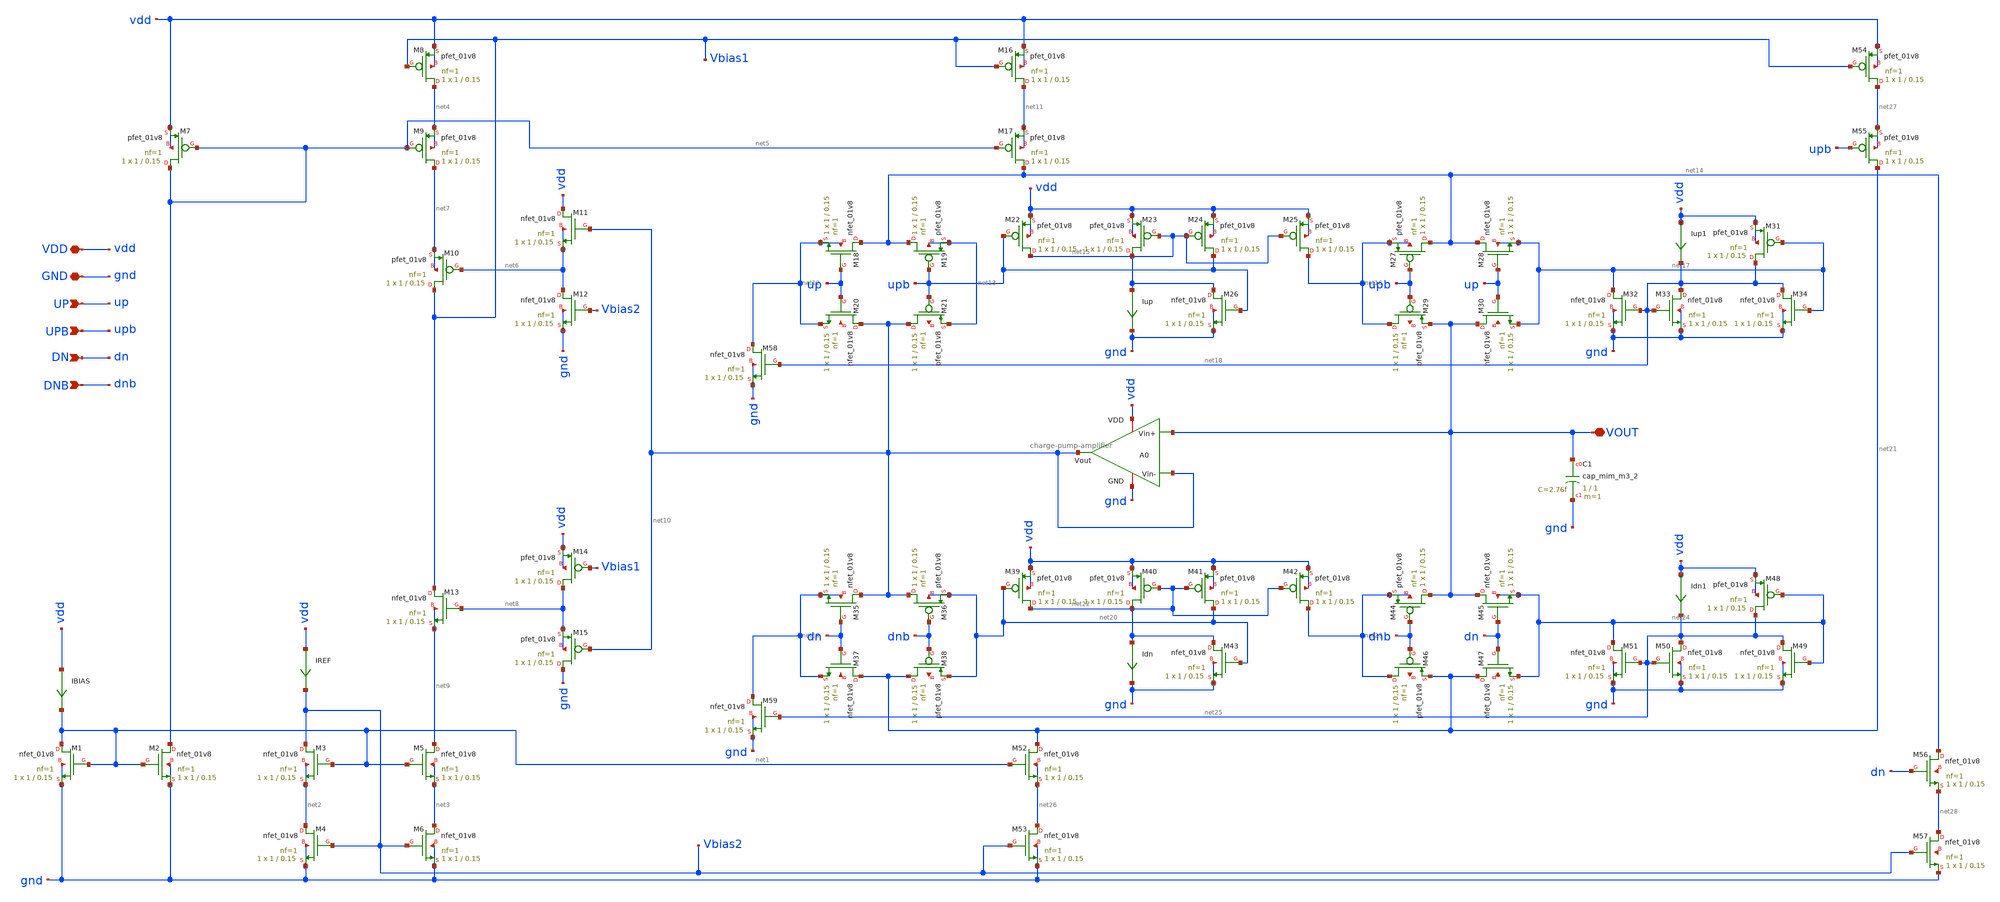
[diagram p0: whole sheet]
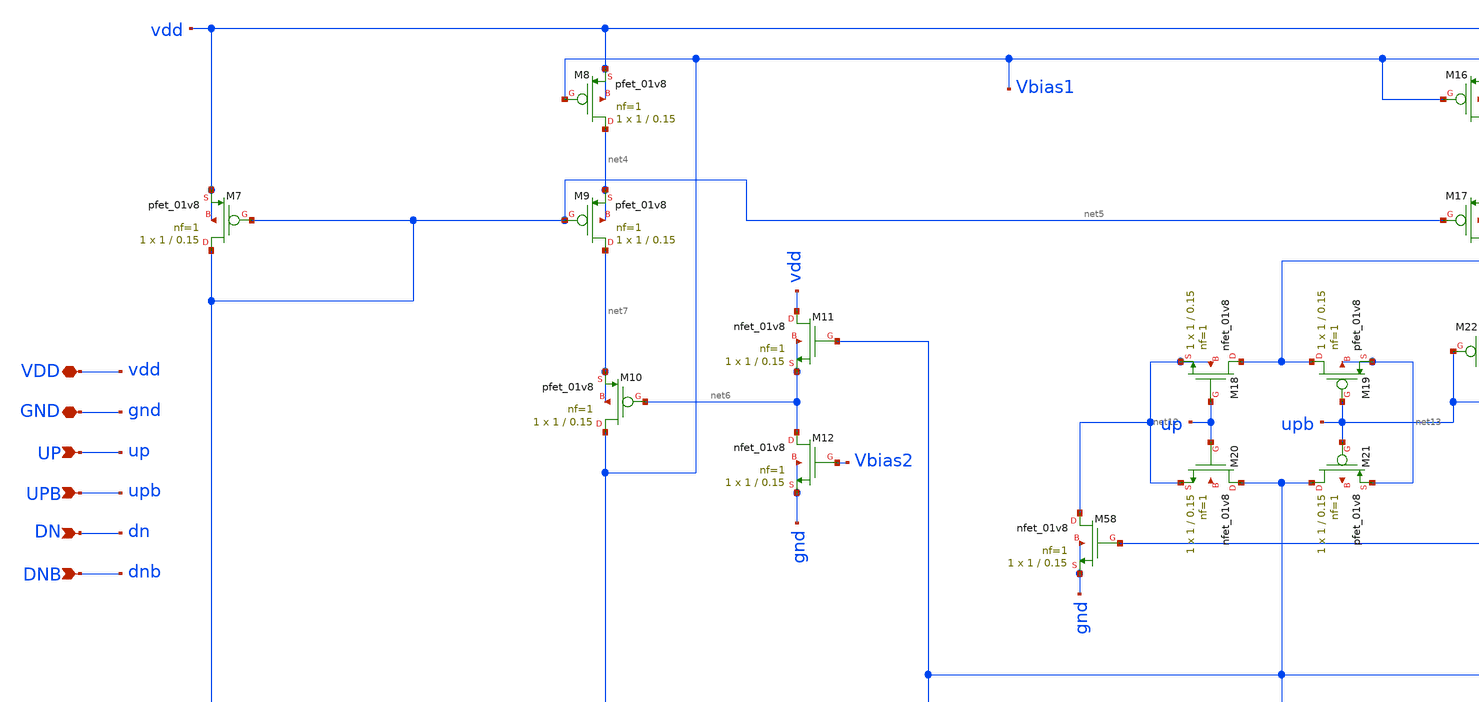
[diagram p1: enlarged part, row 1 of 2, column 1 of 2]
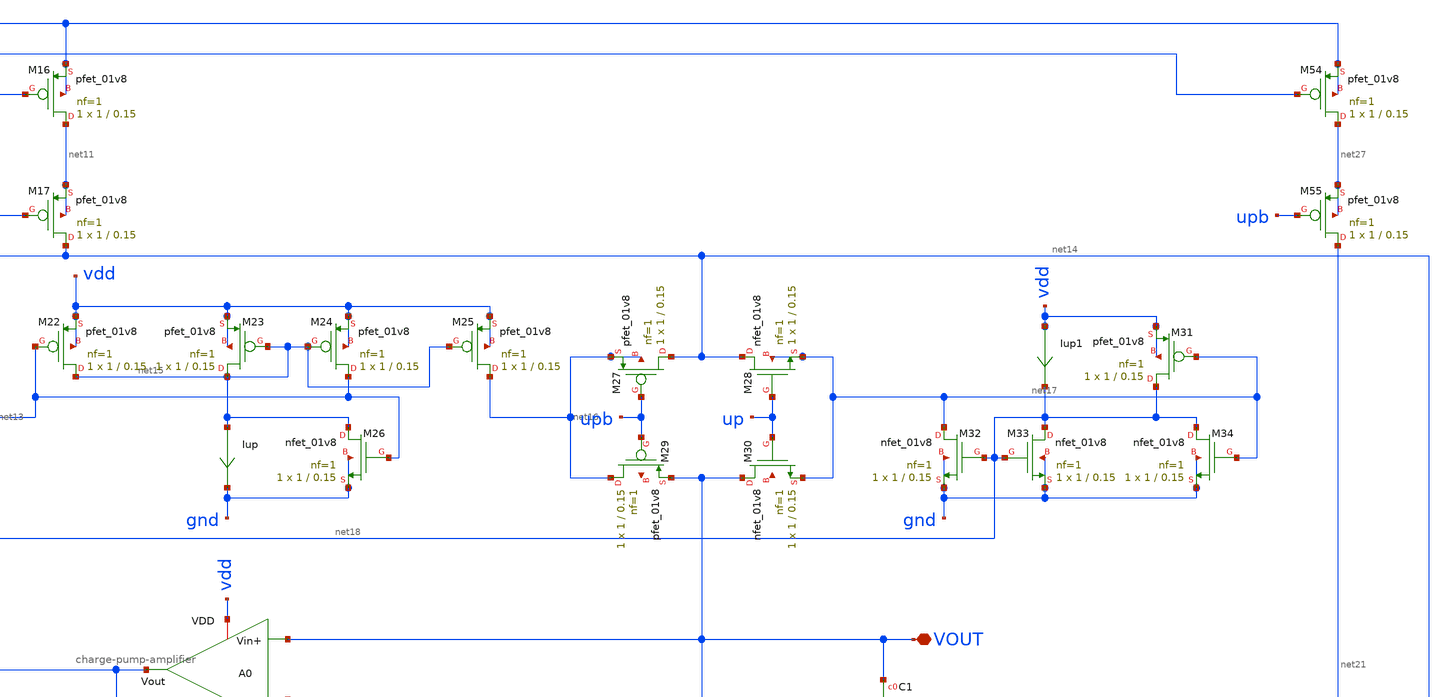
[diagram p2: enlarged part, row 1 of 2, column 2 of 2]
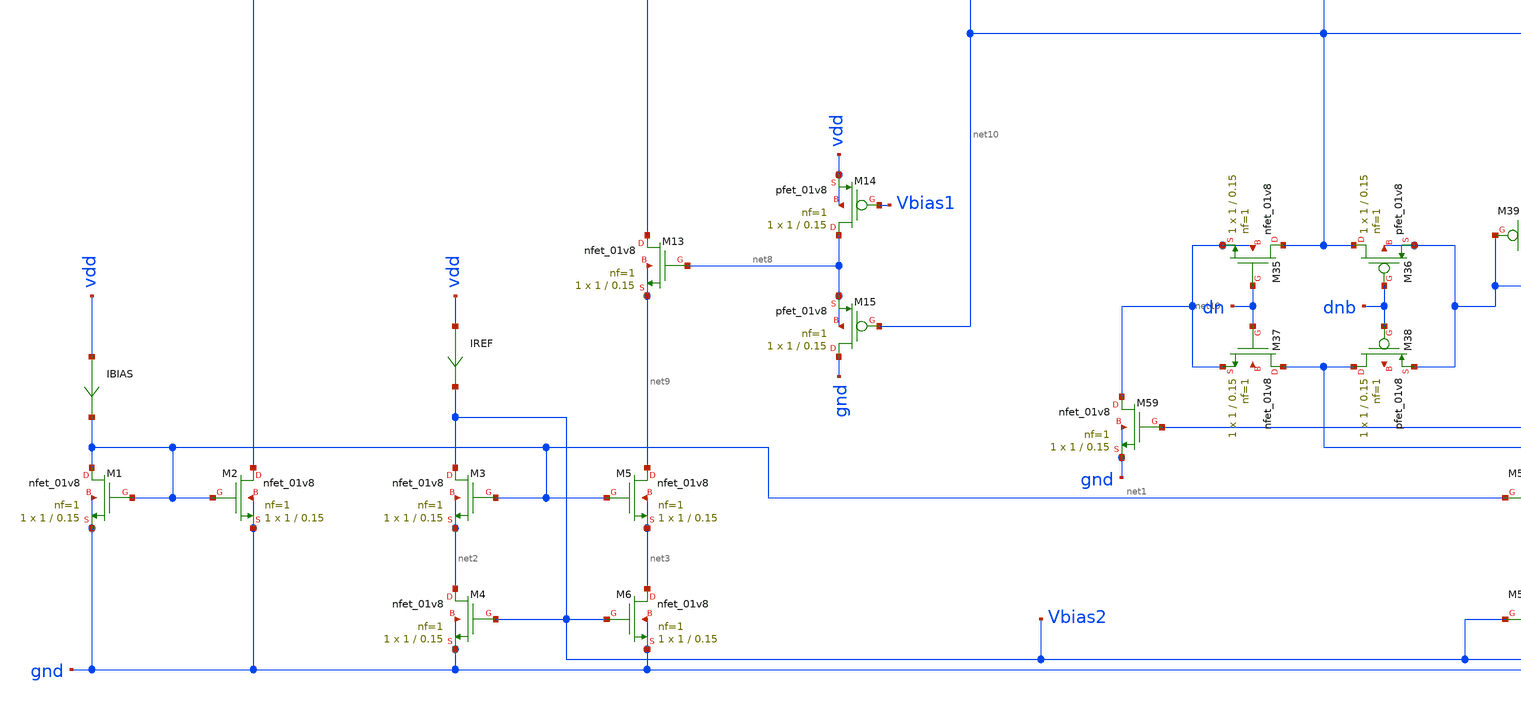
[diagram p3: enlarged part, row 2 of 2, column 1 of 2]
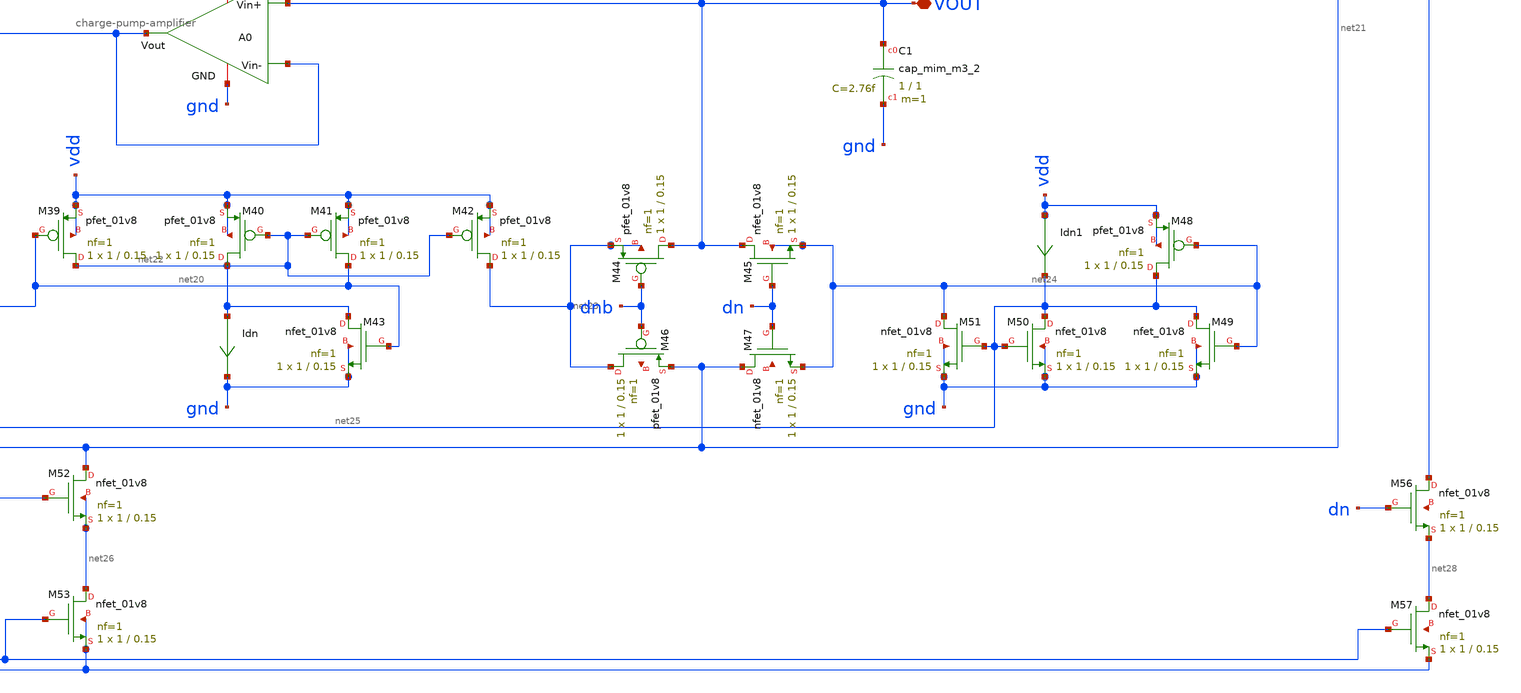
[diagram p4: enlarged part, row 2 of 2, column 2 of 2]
** sch_path: charge-pump/charge-pump.sch
**.subckt charge-pump VOUT DN VDD GND DNB UPB UP
*.iopin VOUT
*.ipin DN
*.iopin VDD
*.iopin GND
*.ipin DNB
*.ipin UPB
*.ipin UP
XM1 net1 net1 gnd gnd sky130_fd_pr__nfet_01v8 L=0.15 W=1 nf=1 ad='int((nf+1)/2) * W/nf * 0.29' as='int((nf+2)/2) * W/nf * 0.29'
+ pd='2*int((nf+1)/2) * (W/nf + 0.29)' ps='2*int((nf+2)/2) * (W/nf + 0.29)' nrd='0.29 / W' nrs='0.29 / W'
+ sa=0 sb=0 sd=0 mult=1 m=1
XM2 net5 net1 gnd gnd sky130_fd_pr__nfet_01v8 L=0.15 W=1 nf=1 ad='int((nf+1)/2) * W/nf * 0.29' as='int((nf+2)/2) * W/nf * 0.29'
+ pd='2*int((nf+1)/2) * (W/nf + 0.29)' ps='2*int((nf+2)/2) * (W/nf + 0.29)' nrd='0.29 / W' nrs='0.29 / W'
+ sa=0 sb=0 sd=0 mult=1 m=1
XM3 Vbias2 net1 net2 net2 sky130_fd_pr__nfet_01v8 L=0.15 W=1 nf=1 ad='int((nf+1)/2) * W/nf * 0.29' as='int((nf+2)/2) * W/nf * 0.29'
+ pd='2*int((nf+1)/2) * (W/nf + 0.29)' ps='2*int((nf+2)/2) * (W/nf + 0.29)' nrd='0.29 / W' nrs='0.29 / W'
+ sa=0 sb=0 sd=0 mult=1 m=1
XM4 net2 Vbias2 gnd gnd sky130_fd_pr__nfet_01v8 L=0.15 W=1 nf=1 ad='int((nf+1)/2) * W/nf * 0.29' as='int((nf+2)/2) * W/nf * 0.29'
+ pd='2*int((nf+1)/2) * (W/nf + 0.29)' ps='2*int((nf+2)/2) * (W/nf + 0.29)' nrd='0.29 / W' nrs='0.29 / W'
+ sa=0 sb=0 sd=0 mult=1 m=1
XM5 net9 net1 net3 net3 sky130_fd_pr__nfet_01v8 L=0.15 W=1 nf=1 ad='int((nf+1)/2) * W/nf * 0.29' as='int((nf+2)/2) * W/nf * 0.29'
+ pd='2*int((nf+1)/2) * (W/nf + 0.29)' ps='2*int((nf+2)/2) * (W/nf + 0.29)' nrd='0.29 / W' nrs='0.29 / W'
+ sa=0 sb=0 sd=0 mult=1 m=1
XM6 net3 Vbias2 gnd gnd sky130_fd_pr__nfet_01v8 L=0.15 W=1 nf=1 ad='int((nf+1)/2) * W/nf * 0.29' as='int((nf+2)/2) * W/nf * 0.29'
+ pd='2*int((nf+1)/2) * (W/nf + 0.29)' ps='2*int((nf+2)/2) * (W/nf + 0.29)' nrd='0.29 / W' nrs='0.29 / W'
+ sa=0 sb=0 sd=0 mult=1 m=1
XM7 net5 net5 vdd vdd sky130_fd_pr__pfet_01v8 L=0.15 W=1 nf=1 ad='int((nf+1)/2) * W/nf * 0.29' as='int((nf+2)/2) * W/nf * 0.29'
+ pd='2*int((nf+1)/2) * (W/nf + 0.29)' ps='2*int((nf+2)/2) * (W/nf + 0.29)' nrd='0.29 / W' nrs='0.29 / W'
+ sa=0 sb=0 sd=0 mult=1 m=1
XM8 net4 Vbias1 vdd vdd sky130_fd_pr__pfet_01v8 L=0.15 W=1 nf=1 ad='int((nf+1)/2) * W/nf * 0.29' as='int((nf+2)/2) * W/nf * 0.29'
+ pd='2*int((nf+1)/2) * (W/nf + 0.29)' ps='2*int((nf+2)/2) * (W/nf + 0.29)' nrd='0.29 / W' nrs='0.29 / W'
+ sa=0 sb=0 sd=0 mult=1 m=1
XM9 net7 net5 net4 net4 sky130_fd_pr__pfet_01v8 L=0.15 W=1 nf=1 ad='int((nf+1)/2) * W/nf * 0.29' as='int((nf+2)/2) * W/nf * 0.29'
+ pd='2*int((nf+1)/2) * (W/nf + 0.29)' ps='2*int((nf+2)/2) * (W/nf + 0.29)' nrd='0.29 / W' nrs='0.29 / W'
+ sa=0 sb=0 sd=0 mult=1 m=1
XM10 Vbias1 net6 net7 net7 sky130_fd_pr__pfet_01v8 L=0.15 W=1 nf=1 ad='int((nf+1)/2) * W/nf * 0.29' as='int((nf+2)/2) * W/nf * 0.29'
+ pd='2*int((nf+1)/2) * (W/nf + 0.29)' ps='2*int((nf+2)/2) * (W/nf + 0.29)' nrd='0.29 / W' nrs='0.29 / W'
+ sa=0 sb=0 sd=0 mult=1 m=1
XM11 vdd net10 net6 net6 sky130_fd_pr__nfet_01v8 L=0.15 W=1 nf=1 ad='int((nf+1)/2) * W/nf * 0.29' as='int((nf+2)/2) * W/nf * 0.29'
+ pd='2*int((nf+1)/2) * (W/nf + 0.29)' ps='2*int((nf+2)/2) * (W/nf + 0.29)' nrd='0.29 / W' nrs='0.29 / W'
+ sa=0 sb=0 sd=0 mult=1 m=1
XM12 net6 Vbias2 gnd gnd sky130_fd_pr__nfet_01v8 L=0.15 W=1 nf=1 ad='int((nf+1)/2) * W/nf * 0.29' as='int((nf+2)/2) * W/nf * 0.29'
+ pd='2*int((nf+1)/2) * (W/nf + 0.29)' ps='2*int((nf+2)/2) * (W/nf + 0.29)' nrd='0.29 / W' nrs='0.29 / W'
+ sa=0 sb=0 sd=0 mult=1 m=1
XM13 Vbias1 net8 net9 net9 sky130_fd_pr__nfet_01v8 L=0.15 W=1 nf=1 ad='int((nf+1)/2) * W/nf * 0.29' as='int((nf+2)/2) * W/nf * 0.29'
+ pd='2*int((nf+1)/2) * (W/nf + 0.29)' ps='2*int((nf+2)/2) * (W/nf + 0.29)' nrd='0.29 / W' nrs='0.29 / W'
+ sa=0 sb=0 sd=0 mult=1 m=1
XM14 net8 Vbias1 vdd vdd sky130_fd_pr__pfet_01v8 L=0.15 W=1 nf=1 ad='int((nf+1)/2) * W/nf * 0.29' as='int((nf+2)/2) * W/nf * 0.29'
+ pd='2*int((nf+1)/2) * (W/nf + 0.29)' ps='2*int((nf+2)/2) * (W/nf + 0.29)' nrd='0.29 / W' nrs='0.29 / W'
+ sa=0 sb=0 sd=0 mult=1 m=1
XM15 gnd net10 net8 net8 sky130_fd_pr__pfet_01v8 L=0.15 W=1 nf=1 ad='int((nf+1)/2) * W/nf * 0.29' as='int((nf+2)/2) * W/nf * 0.29'
+ pd='2*int((nf+1)/2) * (W/nf + 0.29)' ps='2*int((nf+2)/2) * (W/nf + 0.29)' nrd='0.29 / W' nrs='0.29 / W'
+ sa=0 sb=0 sd=0 mult=1 m=1
XM16 net11 Vbias1 vdd vdd sky130_fd_pr__pfet_01v8 L=0.15 W=1 nf=1 ad='int((nf+1)/2) * W/nf * 0.29' as='int((nf+2)/2) * W/nf * 0.29'
+ pd='2*int((nf+1)/2) * (W/nf + 0.29)' ps='2*int((nf+2)/2) * (W/nf + 0.29)' nrd='0.29 / W' nrs='0.29 / W'
+ sa=0 sb=0 sd=0 mult=1 m=1
XM17 net14 net5 net11 net11 sky130_fd_pr__pfet_01v8 L=0.15 W=1 nf=1 ad='int((nf+1)/2) * W/nf * 0.29'
+ as='int((nf+2)/2) * W/nf * 0.29' pd='2*int((nf+1)/2) * (W/nf + 0.29)' ps='2*int((nf+2)/2) * (W/nf + 0.29)'
+ nrd='0.29 / W' nrs='0.29 / W' sa=0 sb=0 sd=0 mult=1 m=1
XM18 net14 up net12 net12 sky130_fd_pr__nfet_01v8 L=0.15 W=1 nf=1 ad='int((nf+1)/2) * W/nf * 0.29' as='int((nf+2)/2) * W/nf * 0.29'
+ pd='2*int((nf+1)/2) * (W/nf + 0.29)' ps='2*int((nf+2)/2) * (W/nf + 0.29)' nrd='0.29 / W' nrs='0.29 / W'
+ sa=0 sb=0 sd=0 mult=1 m=1
XM19 net14 upb net13 net13 sky130_fd_pr__pfet_01v8 L=0.15 W=1 nf=1 ad='int((nf+1)/2) * W/nf * 0.29' as='int((nf+2)/2) * W/nf * 0.29'
+ pd='2*int((nf+1)/2) * (W/nf + 0.29)' ps='2*int((nf+2)/2) * (W/nf + 0.29)' nrd='0.29 / W' nrs='0.29 / W'
+ sa=0 sb=0 sd=0 mult=1 m=1
XM20 net10 up net12 net29 sky130_fd_pr__nfet_01v8 L=0.15 W=1 nf=1 ad='int((nf+1)/2) * W/nf * 0.29' as='int((nf+2)/2) * W/nf * 0.29'
+ pd='2*int((nf+1)/2) * (W/nf + 0.29)' ps='2*int((nf+2)/2) * (W/nf + 0.29)' nrd='0.29 / W' nrs='0.29 / W'
+ sa=0 sb=0 sd=0 mult=1 m=1
XM21 net10 upb net13 net30 sky130_fd_pr__pfet_01v8 L=0.15 W=1 nf=1 ad='int((nf+1)/2) * W/nf * 0.29' as='int((nf+2)/2) * W/nf * 0.29'
+ pd='2*int((nf+1)/2) * (W/nf + 0.29)' ps='2*int((nf+2)/2) * (W/nf + 0.29)' nrd='0.29 / W' nrs='0.29 / W'
+ sa=0 sb=0 sd=0 mult=1 m=1
XM22 net15 upb vdd vdd sky130_fd_pr__pfet_01v8 L=0.15 W=1 nf=1 ad='int((nf+1)/2) * W/nf * 0.29' as='int((nf+2)/2) * W/nf * 0.29'
+ pd='2*int((nf+1)/2) * (W/nf + 0.29)' ps='2*int((nf+2)/2) * (W/nf + 0.29)' nrd='0.29 / W' nrs='0.29 / W'
+ sa=0 sb=0 sd=0 mult=1 m=1
XM23 net15 net15 vdd vdd sky130_fd_pr__pfet_01v8 L=0.15 W=1 nf=1 ad='int((nf+1)/2) * W/nf * 0.29' as='int((nf+2)/2) * W/nf * 0.29'
+ pd='2*int((nf+1)/2) * (W/nf + 0.29)' ps='2*int((nf+2)/2) * (W/nf + 0.29)' nrd='0.29 / W' nrs='0.29 / W'
+ sa=0 sb=0 sd=0 mult=1 m=1
XM24 upb net15 vdd vdd sky130_fd_pr__pfet_01v8 L=0.15 W=1 nf=1 ad='int((nf+1)/2) * W/nf * 0.29' as='int((nf+2)/2) * W/nf * 0.29'
+ pd='2*int((nf+1)/2) * (W/nf + 0.29)' ps='2*int((nf+2)/2) * (W/nf + 0.29)' nrd='0.29 / W' nrs='0.29 / W'
+ sa=0 sb=0 sd=0 mult=1 m=1
XM25 net16 net15 vdd vdd sky130_fd_pr__pfet_01v8 L=0.15 W=1 nf=1 ad='int((nf+1)/2) * W/nf * 0.29' as='int((nf+2)/2) * W/nf * 0.29'
+ pd='2*int((nf+1)/2) * (W/nf + 0.29)' ps='2*int((nf+2)/2) * (W/nf + 0.29)' nrd='0.29 / W' nrs='0.29 / W'
+ sa=0 sb=0 sd=0 mult=1 m=1
XM26 net15 upb gnd gnd sky130_fd_pr__nfet_01v8 L=0.15 W=1 nf=1 ad='int((nf+1)/2) * W/nf * 0.29' as='int((nf+2)/2) * W/nf * 0.29'
+ pd='2*int((nf+1)/2) * (W/nf + 0.29)' ps='2*int((nf+2)/2) * (W/nf + 0.29)' nrd='0.29 / W' nrs='0.29 / W'
+ sa=0 sb=0 sd=0 mult=1 m=1
XM31 net18 net17 vdd vdd sky130_fd_pr__pfet_01v8 L=0.15 W=1 nf=1 ad='int((nf+1)/2) * W/nf * 0.29' as='int((nf+2)/2) * W/nf * 0.29'
+ pd='2*int((nf+1)/2) * (W/nf + 0.29)' ps='2*int((nf+2)/2) * (W/nf + 0.29)' nrd='0.29 / W' nrs='0.29 / W'
+ sa=0 sb=0 sd=0 mult=1 m=1
XM32 net17 net18 gnd gnd sky130_fd_pr__nfet_01v8 L=0.15 W=1 nf=1 ad='int((nf+1)/2) * W/nf * 0.29' as='int((nf+2)/2) * W/nf * 0.29'
+ pd='2*int((nf+1)/2) * (W/nf + 0.29)' ps='2*int((nf+2)/2) * (W/nf + 0.29)' nrd='0.29 / W' nrs='0.29 / W'
+ sa=0 sb=0 sd=0 mult=1 m=1
XM33 net18 net18 gnd gnd sky130_fd_pr__nfet_01v8 L=0.15 W=1 nf=1 ad='int((nf+1)/2) * W/nf * 0.29' as='int((nf+2)/2) * W/nf * 0.29'
+ pd='2*int((nf+1)/2) * (W/nf + 0.29)' ps='2*int((nf+2)/2) * (W/nf + 0.29)' nrd='0.29 / W' nrs='0.29 / W'
+ sa=0 sb=0 sd=0 mult=1 m=1
XM34 net18 net17 gnd gnd sky130_fd_pr__nfet_01v8 L=0.15 W=1 nf=1 ad='int((nf+1)/2) * W/nf * 0.29' as='int((nf+2)/2) * W/nf * 0.29'
+ pd='2*int((nf+1)/2) * (W/nf + 0.29)' ps='2*int((nf+2)/2) * (W/nf + 0.29)' nrd='0.29 / W' nrs='0.29 / W'
+ sa=0 sb=0 sd=0 mult=1 m=1
XM27 net14 upb net16 net16 sky130_fd_pr__pfet_01v8 L=0.15 W=1 nf=1 ad='int((nf+1)/2) * W/nf * 0.29' as='int((nf+2)/2) * W/nf * 0.29'
+ pd='2*int((nf+1)/2) * (W/nf + 0.29)' ps='2*int((nf+2)/2) * (W/nf + 0.29)' nrd='0.29 / W' nrs='0.29 / W'
+ sa=0 sb=0 sd=0 mult=1 m=1
XM28 net14 up net17 net17 sky130_fd_pr__nfet_01v8 L=0.15 W=1 nf=1 ad='int((nf+1)/2) * W/nf * 0.29' as='int((nf+2)/2) * W/nf * 0.29'
+ pd='2*int((nf+1)/2) * (W/nf + 0.29)' ps='2*int((nf+2)/2) * (W/nf + 0.29)' nrd='0.29 / W' nrs='0.29 / W'
+ sa=0 sb=0 sd=0 mult=1 m=1
XM29 net16 upb VOUT net31 sky130_fd_pr__pfet_01v8 L=0.15 W=1 nf=1 ad='int((nf+1)/2) * W/nf * 0.29' as='int((nf+2)/2) * W/nf * 0.29'
+ pd='2*int((nf+1)/2) * (W/nf + 0.29)' ps='2*int((nf+2)/2) * (W/nf + 0.29)' nrd='0.29 / W' nrs='0.29 / W'
+ sa=0 sb=0 sd=0 mult=1 m=1
XM30 VOUT up net17 net32 sky130_fd_pr__nfet_01v8 L=0.15 W=1 nf=1 ad='int((nf+1)/2) * W/nf * 0.29' as='int((nf+2)/2) * W/nf * 0.29'
+ pd='2*int((nf+1)/2) * (W/nf + 0.29)' ps='2*int((nf+2)/2) * (W/nf + 0.29)' nrd='0.29 / W' nrs='0.29 / W'
+ sa=0 sb=0 sd=0 mult=1 m=1
XM35 net10 dn net19 net19 sky130_fd_pr__nfet_01v8 L=0.15 W=1 nf=1 ad='int((nf+1)/2) * W/nf * 0.29' as='int((nf+2)/2) * W/nf * 0.29'
+ pd='2*int((nf+1)/2) * (W/nf + 0.29)' ps='2*int((nf+2)/2) * (W/nf + 0.29)' nrd='0.29 / W' nrs='0.29 / W'
+ sa=0 sb=0 sd=0 mult=1 m=1
XM36 net10 dnb net20 net20 sky130_fd_pr__pfet_01v8 L=0.15 W=1 nf=1 ad='int((nf+1)/2) * W/nf * 0.29' as='int((nf+2)/2) * W/nf * 0.29'
+ pd='2*int((nf+1)/2) * (W/nf + 0.29)' ps='2*int((nf+2)/2) * (W/nf + 0.29)' nrd='0.29 / W' nrs='0.29 / W'
+ sa=0 sb=0 sd=0 mult=1 m=1
XM37 net21 dn net19 net33 sky130_fd_pr__nfet_01v8 L=0.15 W=1 nf=1 ad='int((nf+1)/2) * W/nf * 0.29' as='int((nf+2)/2) * W/nf * 0.29'
+ pd='2*int((nf+1)/2) * (W/nf + 0.29)' ps='2*int((nf+2)/2) * (W/nf + 0.29)' nrd='0.29 / W' nrs='0.29 / W'
+ sa=0 sb=0 sd=0 mult=1 m=1
XM38 net21 dnb net20 net34 sky130_fd_pr__pfet_01v8 L=0.15 W=1 nf=1 ad='int((nf+1)/2) * W/nf * 0.29' as='int((nf+2)/2) * W/nf * 0.29'
+ pd='2*int((nf+1)/2) * (W/nf + 0.29)' ps='2*int((nf+2)/2) * (W/nf + 0.29)' nrd='0.29 / W' nrs='0.29 / W'
+ sa=0 sb=0 sd=0 mult=1 m=1
XM39 net22 net20 vdd vdd sky130_fd_pr__pfet_01v8 L=0.15 W=1 nf=1 ad='int((nf+1)/2) * W/nf * 0.29' as='int((nf+2)/2) * W/nf * 0.29'
+ pd='2*int((nf+1)/2) * (W/nf + 0.29)' ps='2*int((nf+2)/2) * (W/nf + 0.29)' nrd='0.29 / W' nrs='0.29 / W'
+ sa=0 sb=0 sd=0 mult=1 m=1
XM40 net22 net22 vdd vdd sky130_fd_pr__pfet_01v8 L=0.15 W=1 nf=1 ad='int((nf+1)/2) * W/nf * 0.29' as='int((nf+2)/2) * W/nf * 0.29'
+ pd='2*int((nf+1)/2) * (W/nf + 0.29)' ps='2*int((nf+2)/2) * (W/nf + 0.29)' nrd='0.29 / W' nrs='0.29 / W'
+ sa=0 sb=0 sd=0 mult=1 m=1
XM41 net20 net22 vdd vdd sky130_fd_pr__pfet_01v8 L=0.15 W=1 nf=1 ad='int((nf+1)/2) * W/nf * 0.29' as='int((nf+2)/2) * W/nf * 0.29'
+ pd='2*int((nf+1)/2) * (W/nf + 0.29)' ps='2*int((nf+2)/2) * (W/nf + 0.29)' nrd='0.29 / W' nrs='0.29 / W'
+ sa=0 sb=0 sd=0 mult=1 m=1
XM42 net23 net22 vdd vdd sky130_fd_pr__pfet_01v8 L=0.15 W=1 nf=1 ad='int((nf+1)/2) * W/nf * 0.29' as='int((nf+2)/2) * W/nf * 0.29'
+ pd='2*int((nf+1)/2) * (W/nf + 0.29)' ps='2*int((nf+2)/2) * (W/nf + 0.29)' nrd='0.29 / W' nrs='0.29 / W'
+ sa=0 sb=0 sd=0 mult=1 m=1
XM43 net22 net20 gnd gnd sky130_fd_pr__nfet_01v8 L=0.15 W=1 nf=1 ad='int((nf+1)/2) * W/nf * 0.29' as='int((nf+2)/2) * W/nf * 0.29'
+ pd='2*int((nf+1)/2) * (W/nf + 0.29)' ps='2*int((nf+2)/2) * (W/nf + 0.29)' nrd='0.29 / W' nrs='0.29 / W'
+ sa=0 sb=0 sd=0 mult=1 m=1
XM44 VOUT dnb net23 net23 sky130_fd_pr__pfet_01v8 L=0.15 W=1 nf=1 ad='int((nf+1)/2) * W/nf * 0.29' as='int((nf+2)/2) * W/nf * 0.29'
+ pd='2*int((nf+1)/2) * (W/nf + 0.29)' ps='2*int((nf+2)/2) * (W/nf + 0.29)' nrd='0.29 / W' nrs='0.29 / W'
+ sa=0 sb=0 sd=0 mult=1 m=1
XM45 VOUT dn net24 net24 sky130_fd_pr__nfet_01v8 L=0.15 W=1 nf=1 ad='int((nf+1)/2) * W/nf * 0.29' as='int((nf+2)/2) * W/nf * 0.29'
+ pd='2*int((nf+1)/2) * (W/nf + 0.29)' ps='2*int((nf+2)/2) * (W/nf + 0.29)' nrd='0.29 / W' nrs='0.29 / W'
+ sa=0 sb=0 sd=0 mult=1 m=1
XM46 net23 dnb net21 net35 sky130_fd_pr__pfet_01v8 L=0.15 W=1 nf=1 ad='int((nf+1)/2) * W/nf * 0.29' as='int((nf+2)/2) * W/nf * 0.29'
+ pd='2*int((nf+1)/2) * (W/nf + 0.29)' ps='2*int((nf+2)/2) * (W/nf + 0.29)' nrd='0.29 / W' nrs='0.29 / W'
+ sa=0 sb=0 sd=0 mult=1 m=1
XM47 net21 dn net24 net36 sky130_fd_pr__nfet_01v8 L=0.15 W=1 nf=1 ad='int((nf+1)/2) * W/nf * 0.29' as='int((nf+2)/2) * W/nf * 0.29'
+ pd='2*int((nf+1)/2) * (W/nf + 0.29)' ps='2*int((nf+2)/2) * (W/nf + 0.29)' nrd='0.29 / W' nrs='0.29 / W'
+ sa=0 sb=0 sd=0 mult=1 m=1
XM48 net25 net24 vdd vdd sky130_fd_pr__pfet_01v8 L=0.15 W=1 nf=1 ad='int((nf+1)/2) * W/nf * 0.29' as='int((nf+2)/2) * W/nf * 0.29'
+ pd='2*int((nf+1)/2) * (W/nf + 0.29)' ps='2*int((nf+2)/2) * (W/nf + 0.29)' nrd='0.29 / W' nrs='0.29 / W'
+ sa=0 sb=0 sd=0 mult=1 m=1
XM49 net25 net24 gnd gnd sky130_fd_pr__nfet_01v8 L=0.15 W=1 nf=1 ad='int((nf+1)/2) * W/nf * 0.29' as='int((nf+2)/2) * W/nf * 0.29'
+ pd='2*int((nf+1)/2) * (W/nf + 0.29)' ps='2*int((nf+2)/2) * (W/nf + 0.29)' nrd='0.29 / W' nrs='0.29 / W'
+ sa=0 sb=0 sd=0 mult=1 m=1
XM50 net25 net25 gnd gnd sky130_fd_pr__nfet_01v8 L=0.15 W=1 nf=1 ad='int((nf+1)/2) * W/nf * 0.29' as='int((nf+2)/2) * W/nf * 0.29'
+ pd='2*int((nf+1)/2) * (W/nf + 0.29)' ps='2*int((nf+2)/2) * (W/nf + 0.29)' nrd='0.29 / W' nrs='0.29 / W'
+ sa=0 sb=0 sd=0 mult=1 m=1
XM51 net24 net25 gnd gnd sky130_fd_pr__nfet_01v8 L=0.15 W=1 nf=1 ad='int((nf+1)/2) * W/nf * 0.29' as='int((nf+2)/2) * W/nf * 0.29'
+ pd='2*int((nf+1)/2) * (W/nf + 0.29)' ps='2*int((nf+2)/2) * (W/nf + 0.29)' nrd='0.29 / W' nrs='0.29 / W'
+ sa=0 sb=0 sd=0 mult=1 m=1
XM52 net21 net1 net26 net26 sky130_fd_pr__nfet_01v8 L=0.15 W=1 nf=1 ad='int((nf+1)/2) * W/nf * 0.29'
+ as='int((nf+2)/2) * W/nf * 0.29' pd='2*int((nf+1)/2) * (W/nf + 0.29)' ps='2*int((nf+2)/2) * (W/nf + 0.29)'
+ nrd='0.29 / W' nrs='0.29 / W' sa=0 sb=0 sd=0 mult=1 m=1
XM53 net26 Vbias2 gnd gnd sky130_fd_pr__nfet_01v8 L=0.15 W=1 nf=1 ad='int((nf+1)/2) * W/nf * 0.29' as='int((nf+2)/2) * W/nf * 0.29'
+ pd='2*int((nf+1)/2) * (W/nf + 0.29)' ps='2*int((nf+2)/2) * (W/nf + 0.29)' nrd='0.29 / W' nrs='0.29 / W'
+ sa=0 sb=0 sd=0 mult=1 m=1
XM54 net27 Vbias1 vdd vdd sky130_fd_pr__pfet_01v8 L=0.15 W=1 nf=1 ad='int((nf+1)/2) * W/nf * 0.29' as='int((nf+2)/2) * W/nf * 0.29'
+ pd='2*int((nf+1)/2) * (W/nf + 0.29)' ps='2*int((nf+2)/2) * (W/nf + 0.29)' nrd='0.29 / W' nrs='0.29 / W'
+ sa=0 sb=0 sd=0 mult=1 m=1
XM55 net21 upb net27 net27 sky130_fd_pr__pfet_01v8 L=0.15 W=1 nf=1 ad='int((nf+1)/2) * W/nf * 0.29' as='int((nf+2)/2) * W/nf * 0.29'
+ pd='2*int((nf+1)/2) * (W/nf + 0.29)' ps='2*int((nf+2)/2) * (W/nf + 0.29)' nrd='0.29 / W' nrs='0.29 / W'
+ sa=0 sb=0 sd=0 mult=1 m=1
XM56 net14 dn net28 net37 sky130_fd_pr__nfet_01v8 L=0.15 W=1 nf=1 ad='int((nf+1)/2) * W/nf * 0.29' as='int((nf+2)/2) * W/nf * 0.29'
+ pd='2*int((nf+1)/2) * (W/nf + 0.29)' ps='2*int((nf+2)/2) * (W/nf + 0.29)' nrd='0.29 / W' nrs='0.29 / W'
+ sa=0 sb=0 sd=0 mult=1 m=1
XM57 net28 Vbias2 gnd net38 sky130_fd_pr__nfet_01v8 L=0.15 W=1 nf=1 ad='int((nf+1)/2) * W/nf * 0.29'
+ as='int((nf+2)/2) * W/nf * 0.29' pd='2*int((nf+1)/2) * (W/nf + 0.29)' ps='2*int((nf+2)/2) * (W/nf + 0.29)'
+ nrd='0.29 / W' nrs='0.29 / W' sa=0 sb=0 sd=0 mult=1 m=1
XM58 net12 net18 gnd gnd sky130_fd_pr__nfet_01v8 L=0.15 W=1 nf=1 ad='int((nf+1)/2) * W/nf * 0.29' as='int((nf+2)/2) * W/nf * 0.29'
+ pd='2*int((nf+1)/2) * (W/nf + 0.29)' ps='2*int((nf+2)/2) * (W/nf + 0.29)' nrd='0.29 / W' nrs='0.29 / W'
+ sa=0 sb=0 sd=0 mult=1 m=1
XM59 net19 net25 gnd gnd sky130_fd_pr__nfet_01v8 L=0.15 W=1 nf=1 ad='int((nf+1)/2) * W/nf * 0.29' as='int((nf+2)/2) * W/nf * 0.29'
+ pd='2*int((nf+1)/2) * (W/nf + 0.29)' ps='2*int((nf+2)/2) * (W/nf + 0.29)' nrd='0.29 / W' nrs='0.29 / W'
+ sa=0 sb=0 sd=0 mult=1 m=1
IBIAS vdd net1 0
.save i(ibias)
IREF vdd Vbias2 0
.save i(iref)
Iup net15 gnd 0
.save i(iup)
Iup1 vdd net18 0
.save i(iup1)
Idn net22 gnd 0
.save i(idn)
Idn1 vdd net25 0
.save i(idn1)
A0 vdd net10 VOUT net10 gnd charge-pump-amplifier
XC1 VOUT gnd sky130_fd_pr__cap_mim_m3_2 W=1 L=1 MF=1 m=1
**.ends

* expanding   symbol:  /home/kenrendell/Playground/IC-design/PLL/charge-pump-amplifier.sym # of
*+ pins=5
** sym_path: charge-pump/charge-pump-amplifier.sym
** sch_path: charge-pump/charge-pump-amplifier.sch
.subckt charge-pump-amplifier VDD Vout Vin+ Vin- GND
*.ipin Vin+
*.ipin Vin-
*.opin Vout
*.iopin VDD
*.iopin GND
XM1p net8 net4 net1 net1 sky130_fd_pr__pfet_01v8 L=0.15 W=1 nf=1 ad='int((nf+1)/2) * W/nf * 0.29' as='int((nf+2)/2) * W/nf * 0.29'
+ pd='2*int((nf+1)/2) * (W/nf + 0.29)' ps='2*int((nf+2)/2) * (W/nf + 0.29)' nrd='0.29 / W' nrs='0.29 / W'
+ sa=0 sb=0 sd=0 mult=1 m=1
XM1n net7 Vin+ net2 net2 sky130_fd_pr__nfet_01v8 L=0.15 W=1 nf=1 ad='int((nf+1)/2) * W/nf * 0.29' as='int((nf+2)/2) * W/nf * 0.29'
+ pd='2*int((nf+1)/2) * (W/nf + 0.29)' ps='2*int((nf+2)/2) * (W/nf + 0.29)' nrd='0.29 / W' nrs='0.29 / W'
+ sa=0 sb=0 sd=0 mult=1 m=1
XM2n net6 Vin- net2 net2 sky130_fd_pr__nfet_01v8 L=0.15 W=1 nf=1 ad='int((nf+1)/2) * W/nf * 0.29' as='int((nf+2)/2) * W/nf * 0.29'
+ pd='2*int((nf+1)/2) * (W/nf + 0.29)' ps='2*int((nf+2)/2) * (W/nf + 0.29)' nrd='0.29 / W' nrs='0.29 / W'
+ sa=0 sb=0 sd=0 mult=1 m=1
XM2p net9 net5 net1 net1 sky130_fd_pr__pfet_01v8 L=0.15 W=1 nf=1 ad='int((nf+1)/2) * W/nf * 0.29' as='int((nf+2)/2) * W/nf * 0.29'
+ pd='2*int((nf+1)/2) * (W/nf + 0.29)' ps='2*int((nf+2)/2) * (W/nf + 0.29)' nrd='0.29 / W' nrs='0.29 / W'
+ sa=0 sb=0 sd=0 mult=1 m=1
XM3 net3 net3 VDD VDD sky130_fd_pr__pfet_01v8 L=0.15 W=1 nf=1 ad='int((nf+1)/2) * W/nf * 0.29' as='int((nf+2)/2) * W/nf * 0.29'
+ pd='2*int((nf+1)/2) * (W/nf + 0.29)' ps='2*int((nf+2)/2) * (W/nf + 0.29)' nrd='0.29 / W' nrs='0.29 / W'
+ sa=0 sb=0 sd=0 mult=1 m=1
XM4 VDD Vin+ net4 net4 sky130_fd_pr__nfet_01v8 L=0.15 W=1 nf=1 ad='int((nf+1)/2) * W/nf * 0.29' as='int((nf+2)/2) * W/nf * 0.29'
+ pd='2*int((nf+1)/2) * (W/nf + 0.29)' ps='2*int((nf+2)/2) * (W/nf + 0.29)' nrd='0.29 / W' nrs='0.29 / W'
+ sa=0 sb=0 sd=0 mult=1 m=1
XM5 net1 net3 VDD VDD sky130_fd_pr__pfet_01v8 L=0.15 W=1 nf=1 ad='int((nf+1)/2) * W/nf * 0.29' as='int((nf+2)/2) * W/nf * 0.29'
+ pd='2*int((nf+1)/2) * (W/nf + 0.29)' ps='2*int((nf+2)/2) * (W/nf + 0.29)' nrd='0.29 / W' nrs='0.29 / W'
+ sa=0 sb=0 sd=0 mult=1 m=1
XM6 net7 net7 VDD VDD sky130_fd_pr__pfet_01v8 L=0.15 W=1 nf=1 ad='int((nf+1)/2) * W/nf * 0.29' as='int((nf+2)/2) * W/nf * 0.29'
+ pd='2*int((nf+1)/2) * (W/nf + 0.29)' ps='2*int((nf+2)/2) * (W/nf + 0.29)' nrd='0.29 / W' nrs='0.29 / W'
+ sa=0 sb=0 sd=0 mult=1 m=1
XM7 net6 net6 VDD VDD sky130_fd_pr__pfet_01v8 L=0.15 W=1 nf=1 ad='int((nf+1)/2) * W/nf * 0.29' as='int((nf+2)/2) * W/nf * 0.29'
+ pd='2*int((nf+1)/2) * (W/nf + 0.29)' ps='2*int((nf+2)/2) * (W/nf + 0.29)' nrd='0.29 / W' nrs='0.29 / W'
+ sa=0 sb=0 sd=0 mult=1 m=1
XM8 VDD Vin- net5 net5 sky130_fd_pr__nfet_01v8 L=0.15 W=1 nf=1 ad='int((nf+1)/2) * W/nf * 0.29' as='int((nf+2)/2) * W/nf * 0.29'
+ pd='2*int((nf+1)/2) * (W/nf + 0.29)' ps='2*int((nf+2)/2) * (W/nf + 0.29)' nrd='0.29 / W' nrs='0.29 / W'
+ sa=0 sb=0 sd=0 mult=1 m=1
XM9 net9 net7 VDD VDD sky130_fd_pr__pfet_01v8 L=0.15 W=1 nf=1 ad='int((nf+1)/2) * W/nf * 0.29' as='int((nf+2)/2) * W/nf * 0.29'
+ pd='2*int((nf+1)/2) * (W/nf + 0.29)' ps='2*int((nf+2)/2) * (W/nf + 0.29)' nrd='0.29 / W' nrs='0.29 / W'
+ sa=0 sb=0 sd=0 mult=1 m=1
XM10 net8 net6 VDD VDD sky130_fd_pr__pfet_01v8 L=0.15 W=1 nf=1 ad='int((nf+1)/2) * W/nf * 0.29' as='int((nf+2)/2) * W/nf * 0.29'
+ pd='2*int((nf+1)/2) * (W/nf + 0.29)' ps='2*int((nf+2)/2) * (W/nf + 0.29)' nrd='0.29 / W' nrs='0.29 / W'
+ sa=0 sb=0 sd=0 mult=1 m=1
XM11 net10 net3 VDD VDD sky130_fd_pr__pfet_01v8 L=0.15 W=1 nf=1 ad='int((nf+1)/2) * W/nf * 0.29' as='int((nf+2)/2) * W/nf * 0.29'
+ pd='2*int((nf+1)/2) * (W/nf + 0.29)' ps='2*int((nf+2)/2) * (W/nf + 0.29)' nrd='0.29 / W' nrs='0.29 / W'
+ sa=0 sb=0 sd=0 mult=1 m=1
XM12 net11 net3 VDD VDD sky130_fd_pr__pfet_01v8 L=0.15 W=1 nf=1 ad='int((nf+1)/2) * W/nf * 0.29' as='int((nf+2)/2) * W/nf * 0.29'
+ pd='2*int((nf+1)/2) * (W/nf + 0.29)' ps='2*int((nf+2)/2) * (W/nf + 0.29)' nrd='0.29 / W' nrs='0.29 / W'
+ sa=0 sb=0 sd=0 mult=1 m=1
XM13 net10 VDD net9 net9 sky130_fd_pr__nfet_01v8 L=0.15 W=1 nf=1 ad='int((nf+1)/2) * W/nf * 0.29' as='int((nf+2)/2) * W/nf * 0.29'
+ pd='2*int((nf+1)/2) * (W/nf + 0.29)' ps='2*int((nf+2)/2) * (W/nf + 0.29)' nrd='0.29 / W' nrs='0.29 / W'
+ sa=0 sb=0 sd=0 mult=1 m=1
XM14 net11 VDD net8 net8 sky130_fd_pr__nfet_01v8 L=0.15 W=1 nf=1 ad='int((nf+1)/2) * W/nf * 0.29' as='int((nf+2)/2) * W/nf * 0.29'
+ pd='2*int((nf+1)/2) * (W/nf + 0.29)' ps='2*int((nf+2)/2) * (W/nf + 0.29)' nrd='0.29 / W' nrs='0.29 / W'
+ sa=0 sb=0 sd=0 mult=1 m=1
XM15 Vout net3 VDD VDD sky130_fd_pr__pfet_01v8 L=0.15 W=1 nf=1 ad='int((nf+1)/2) * W/nf * 0.29' as='int((nf+2)/2) * W/nf * 0.29'
+ pd='2*int((nf+1)/2) * (W/nf + 0.29)' ps='2*int((nf+2)/2) * (W/nf + 0.29)' nrd='0.29 / W' nrs='0.29 / W'
+ sa=0 sb=0 sd=0 mult=1 m=1
XM16 net10 net10 GND net13 sky130_fd_pr__nfet_01v8 L=0.15 W=1 nf=1 ad='int((nf+1)/2) * W/nf * 0.29' as='int((nf+2)/2) * W/nf * 0.29'
+ pd='2*int((nf+1)/2) * (W/nf + 0.29)' ps='2*int((nf+2)/2) * (W/nf + 0.29)' nrd='0.29 / W' nrs='0.29 / W'
+ sa=0 sb=0 sd=0 mult=1 m=1
XM17 net4 net10 GND GND sky130_fd_pr__nfet_01v8 L=0.15 W=1 nf=1 ad='int((nf+1)/2) * W/nf * 0.29' as='int((nf+2)/2) * W/nf * 0.29'
+ pd='2*int((nf+1)/2) * (W/nf + 0.29)' ps='2*int((nf+2)/2) * (W/nf + 0.29)' nrd='0.29 / W' nrs='0.29 / W'
+ sa=0 sb=0 sd=0 mult=1 m=1
XM18 net2 net10 GND GND sky130_fd_pr__nfet_01v8 L=0.15 W=1 nf=1 ad='int((nf+1)/2) * W/nf * 0.29' as='int((nf+2)/2) * W/nf * 0.29'
+ pd='2*int((nf+1)/2) * (W/nf + 0.29)' ps='2*int((nf+2)/2) * (W/nf + 0.29)' nrd='0.29 / W' nrs='0.29 / W'
+ sa=0 sb=0 sd=0 mult=1 m=1
XM19 net5 net10 GND GND sky130_fd_pr__nfet_01v8 L=0.15 W=1 nf=1 ad='int((nf+1)/2) * W/nf * 0.29' as='int((nf+2)/2) * W/nf * 0.29'
+ pd='2*int((nf+1)/2) * (W/nf + 0.29)' ps='2*int((nf+2)/2) * (W/nf + 0.29)' nrd='0.29 / W' nrs='0.29 / W'
+ sa=0 sb=0 sd=0 mult=1 m=1
XM20 net9 net10 GND GND sky130_fd_pr__nfet_01v8 L=0.15 W=1 nf=1 ad='int((nf+1)/2) * W/nf * 0.29' as='int((nf+2)/2) * W/nf * 0.29'
+ pd='2*int((nf+1)/2) * (W/nf + 0.29)' ps='2*int((nf+2)/2) * (W/nf + 0.29)' nrd='0.29 / W' nrs='0.29 / W'
+ sa=0 sb=0 sd=0 mult=1 m=1
XM21 net8 net10 GND GND sky130_fd_pr__nfet_01v8 L=0.15 W=1 nf=1 ad='int((nf+1)/2) * W/nf * 0.29' as='int((nf+2)/2) * W/nf * 0.29'
+ pd='2*int((nf+1)/2) * (W/nf + 0.29)' ps='2*int((nf+2)/2) * (W/nf + 0.29)' nrd='0.29 / W' nrs='0.29 / W'
+ sa=0 sb=0 sd=0 mult=1 m=1
XM22 Vout net11 GND GND sky130_fd_pr__nfet_01v8 L=0.15 W=1 nf=1 ad='int((nf+1)/2) * W/nf * 0.29' as='int((nf+2)/2) * W/nf * 0.29'
+ pd='2*int((nf+1)/2) * (W/nf + 0.29)' ps='2*int((nf+2)/2) * (W/nf + 0.29)' nrd='0.29 / W' nrs='0.29 / W'
+ sa=0 sb=0 sd=0 mult=1 m=1
Rb1 GND net3 sky130_fd_pr__res_generic_l1 W=1 L=1 m=1
Rb2 net10 VDD sky130_fd_pr__res_generic_l1 W=1 L=1 m=1
Rm net12 net11 sky130_fd_pr__res_generic_l1 W=1 L=1 m=1
XCm net12 Vout sky130_fd_pr__cap_mim_m3_2 W=1 L=1 MF=1 m=1
XCL Vout GND sky130_fd_pr__cap_mim_m3_2 W=1 L=1 MF=1 m=1
.ends

.end
